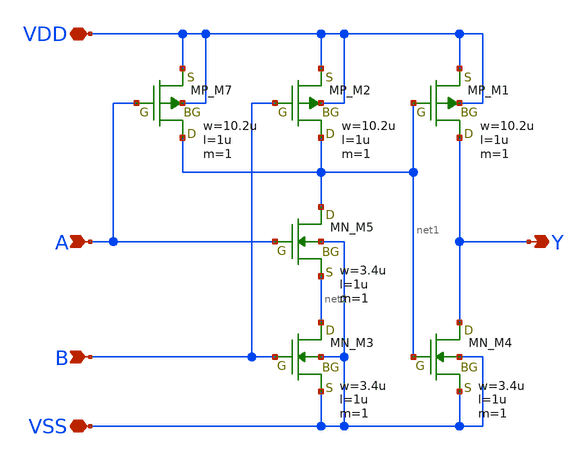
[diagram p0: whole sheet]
** sch_path: member_project/imager/YuMaehashi/design/pulsegen_and2.sch
**.subckt pulsegen_and2 A B VDD VSS Y
*.ipin A
*.ipin B
*.iopin VDD
*.iopin VSS
*.opin Y
XM7 net1 A VDD VDD PMOS w=10.2u l=1u as=0 ad=0 ps=0 pd=0 nrd=0 nrs=0 m=1
XM2 net1 B VDD VDD PMOS w=10.2u l=1u as=0 ad=0 ps=0 pd=0 nrd=0 nrs=0 m=1
XM3 net2 B VSS VSS NMOS w=3.4u l=1u as=0 ad=0 ps=0 pd=0 nrd=0 nrs=0 m=1
XM5 net1 A net2 VSS NMOS w=3.4u l=1u as=0 ad=0 ps=0 pd=0 nrd=0 nrs=0 m=1
XM1 Y net1 VDD VDD PMOS w=10.2u l=1u as=0 ad=0 ps=0 pd=0 nrd=0 nrs=0 m=1
XM4 Y net1 VSS VSS NMOS w=3.4u l=1u as=0 ad=0 ps=0 pd=0 nrd=0 nrs=0 m=1
**.ends
.end
